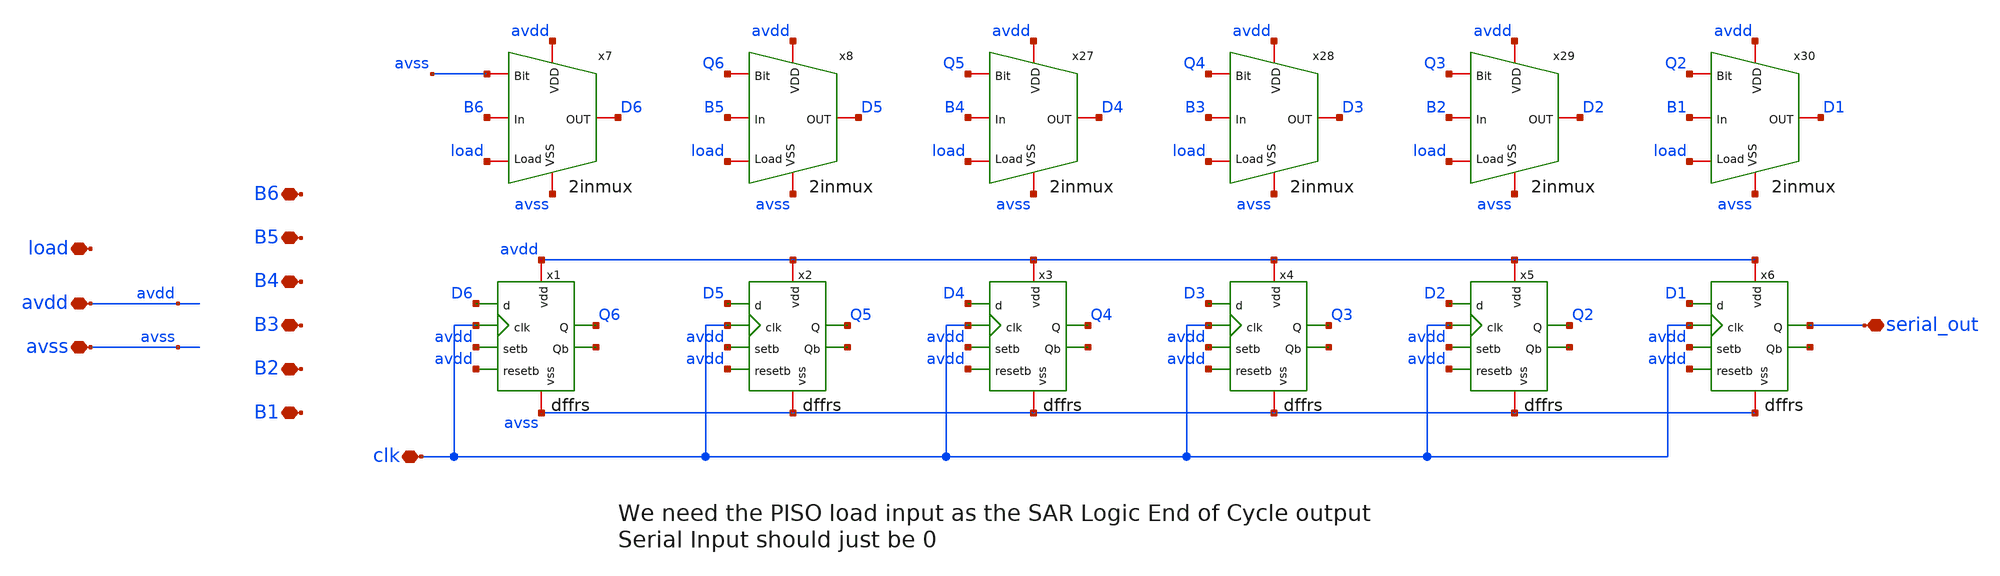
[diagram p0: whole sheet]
** sch_path: designs/FinalBlocksLayout/piso/adc_PISO.sch
**.subckt adc_PISO avdd avss clk B6 B5 B4 B3 B2 B1 load serial_out
*.iopin avdd
*.iopin avss
*.iopin clk
*.iopin B6
*.iopin B5
*.iopin B4
*.iopin B3
*.iopin B2
*.iopin B1
*.iopin load
*.iopin serial_out
x7 avss load avdd D6 avss B6 2inmux
x8 Q6 load avdd D5 avss B5 2inmux
x27 Q5 load avdd D4 avss B4 2inmux
x28 Q4 load avdd D3 avss B3 2inmux
x29 Q3 load avdd D2 avss B2 2inmux
x30 Q2 load avdd D1 avss B1 2inmux
x1 avdd avss D6 clk avdd avdd Q6 net1 dffrs
x2 avdd avss D5 clk avdd avdd Q5 net2 dffrs
x3 avdd avss D4 clk avdd avdd Q4 net3 dffrs
x4 avdd avss D3 clk avdd avdd Q3 net4 dffrs
x5 avdd avss D2 clk avdd avdd Q2 net5 dffrs
x6 avdd avss D1 clk avdd avdd serial_out net6 dffrs
**.ends
.end
